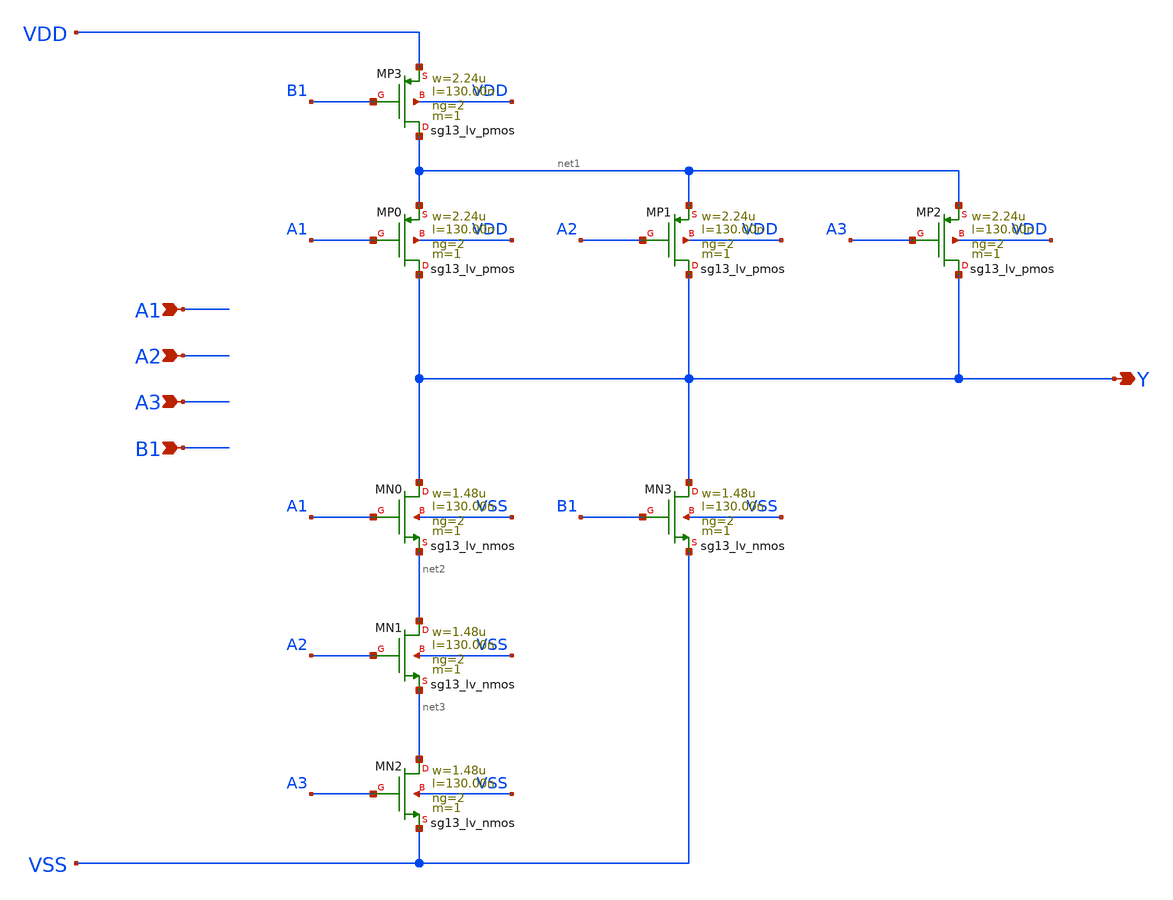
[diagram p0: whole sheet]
** sch_path: outputs/sg13g2_cells/cells/sg13g2_a31oi_2/sg13g2_a31oi_2.sch
**.subckt sg13g2_a31oi_2 A1 A2 A3 B1 Y
*.ipin A1
*.ipin A2
*.ipin A3
*.ipin B1
*.opin Y
XMN0 Y A1 net2 VSS sg13_lv_nmos w=1.48u l=130.00n ng=2 m=1 mm_ok=1
XMN1 net2 A2 net3 VSS sg13_lv_nmos w=1.48u l=130.00n ng=2 m=1 mm_ok=1
XMN2 net3 A3 VSS VSS sg13_lv_nmos w=1.48u l=130.00n ng=2 m=1 mm_ok=1
XMN3 Y B1 VSS VSS sg13_lv_nmos w=1.48u l=130.00n ng=2 m=1 mm_ok=1
XMP0 Y A1 net1 VDD sg13_lv_pmos w=2.24u l=130.00n ng=2 m=1 mm_ok=1
XMP1 Y A2 net1 VDD sg13_lv_pmos w=2.24u l=130.00n ng=2 m=1 mm_ok=1
XMP2 Y A3 net1 VDD sg13_lv_pmos w=2.24u l=130.00n ng=2 m=1 mm_ok=1
XMP3 net1 B1 VDD VDD sg13_lv_pmos w=2.24u l=130.00n ng=2 m=1 mm_ok=1
**.ends
.end
